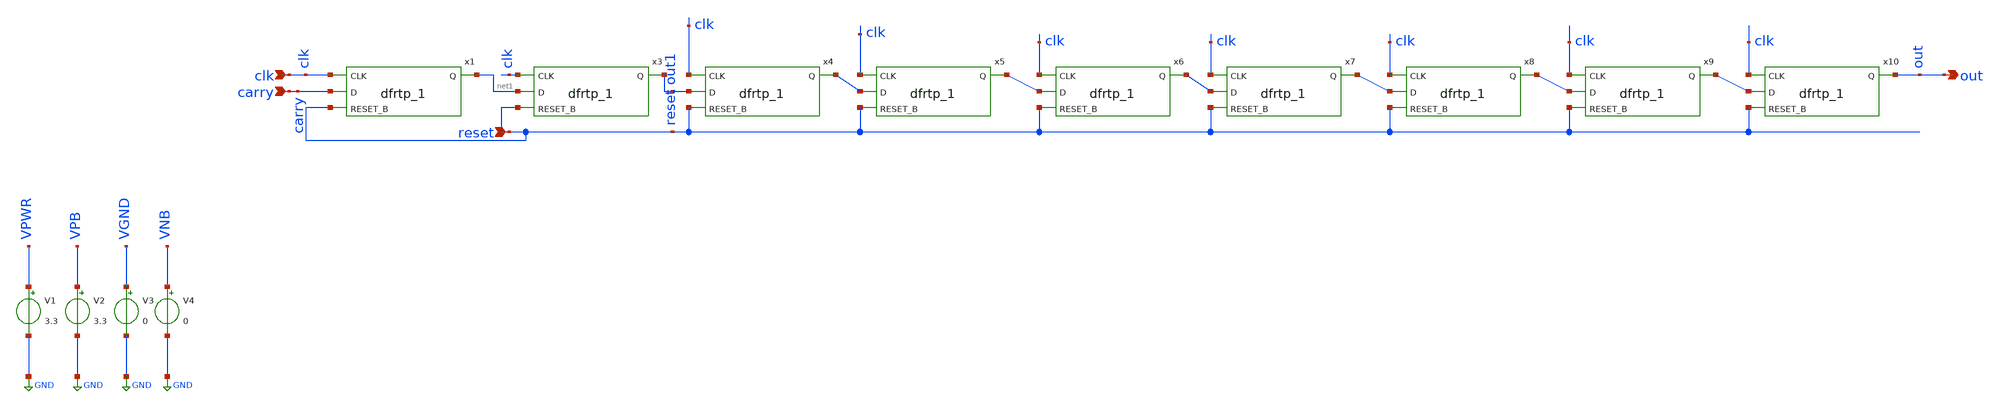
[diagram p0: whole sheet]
** sch_path: xschem/FDC/carry3.51.sch
**.subckt carry3.51 clk reset carry out
*.ipin clk
*.ipin reset
*.ipin carry
*.opin out
x1 clk carry reset VGND VNB VPB VPWR net1 sky130_fd_sc_hvl__dfrtp_1
x3 clk net1 reset VGND VNB VPB VPWR out1 sky130_fd_sc_hvl__dfrtp_1
x4 clk out1 reset VGND VNB VPB VPWR net2 sky130_fd_sc_hvl__dfrtp_1
x5 clk net2 reset VGND VNB VPB VPWR net3 sky130_fd_sc_hvl__dfrtp_1
x6 clk net3 reset VGND VNB VPB VPWR net4 sky130_fd_sc_hvl__dfrtp_1
x7 clk net4 reset VGND VNB VPB VPWR net5 sky130_fd_sc_hvl__dfrtp_1
x8 clk net5 reset VGND VNB VPB VPWR net6 sky130_fd_sc_hvl__dfrtp_1
x9 clk net6 reset VGND VNB VPB VPWR net7 sky130_fd_sc_hvl__dfrtp_1
x10 clk net7 reset VGND VNB VPB VPWR out sky130_fd_sc_hvl__dfrtp_1
V1 VPWR GND 3.3
V2 VPB GND 3.3
V3 VGND GND 0
V4 VNB GND 0
**** begin user architecture code

.lib ~/open_pdks/sky130/sky130A/libs.tech/ngspice/sky130.lib.spice tt
.include /home/vinodhini/open_pdks/sky130/sky130A/libs.ref/sky130_fd_sc_hvl/spice/sky130_fd_sc_hvl.spice

*.MODEL swmod SW(VT=0.0 VH=0.01 RON=1 ROFF=10000000000)
.param mc_mm_switch=0
.param mc_pr_switch=0


.tran 2.5u 1m
.options gmin=1E-11
.save carry reset clk clk1 out

**** end user architecture code
**.ends
.GLOBAL GND
.end
